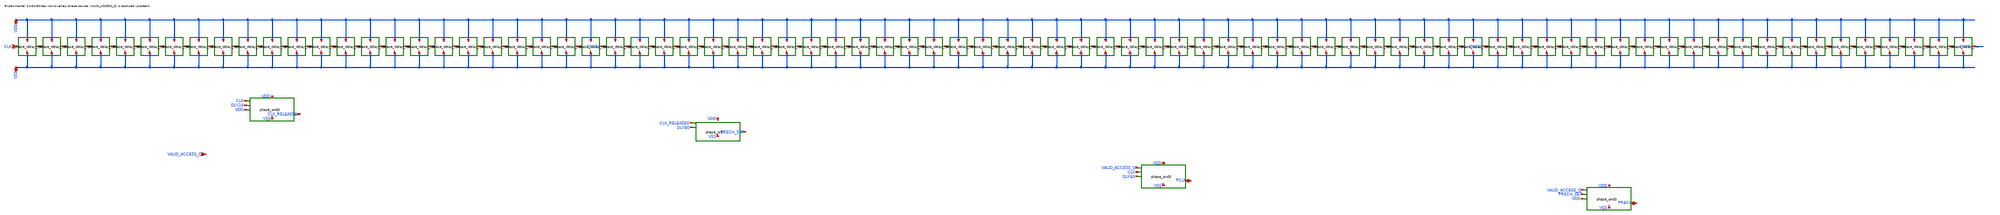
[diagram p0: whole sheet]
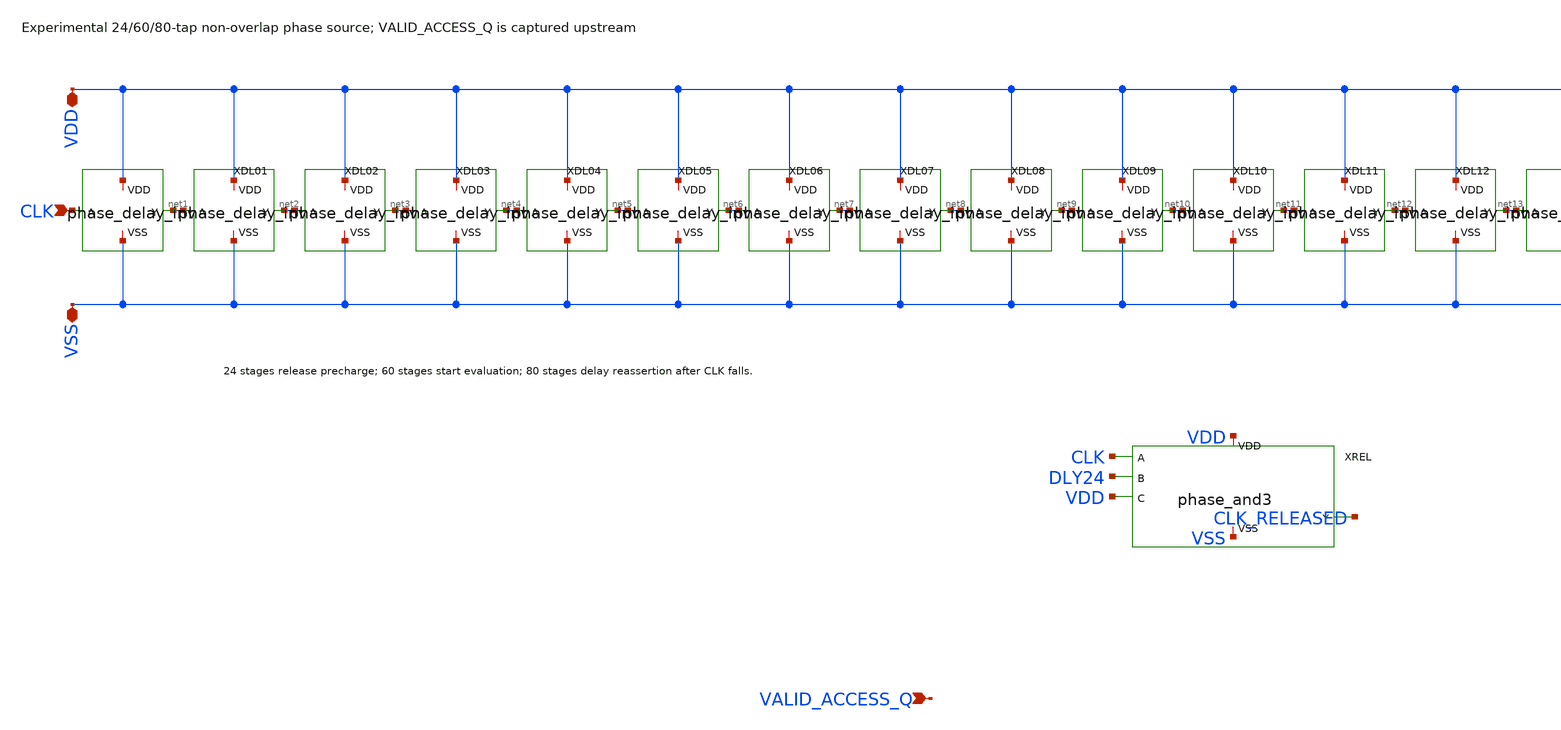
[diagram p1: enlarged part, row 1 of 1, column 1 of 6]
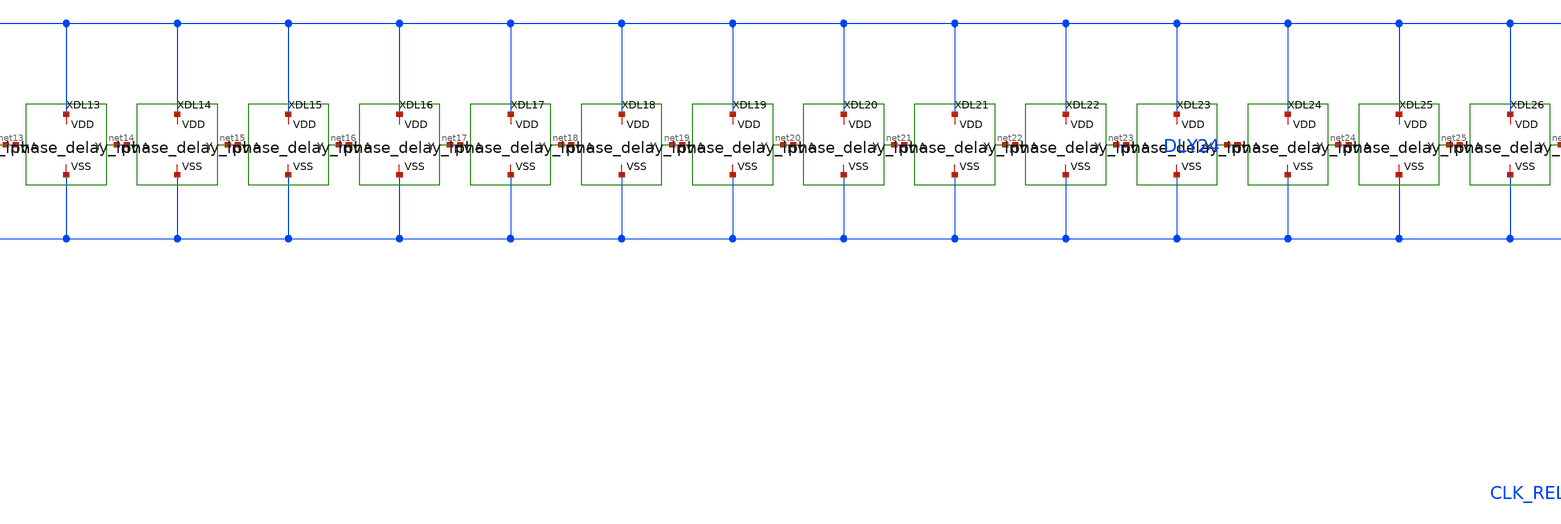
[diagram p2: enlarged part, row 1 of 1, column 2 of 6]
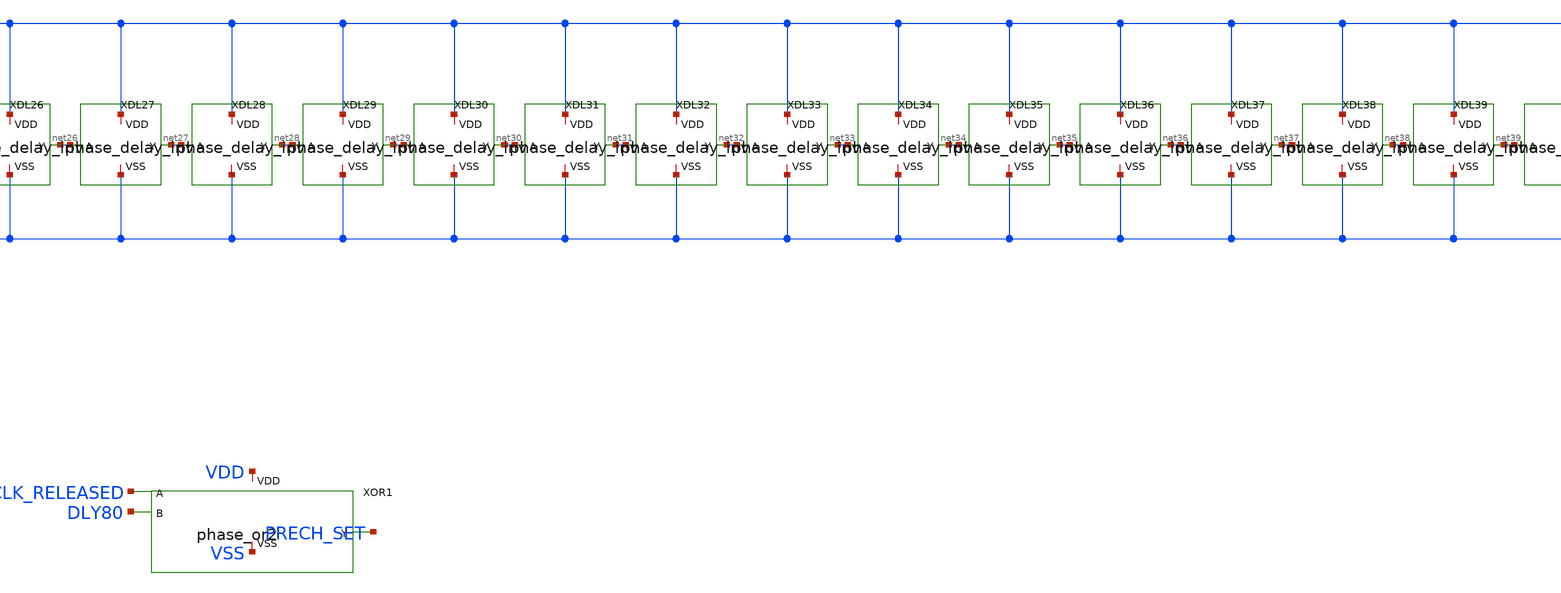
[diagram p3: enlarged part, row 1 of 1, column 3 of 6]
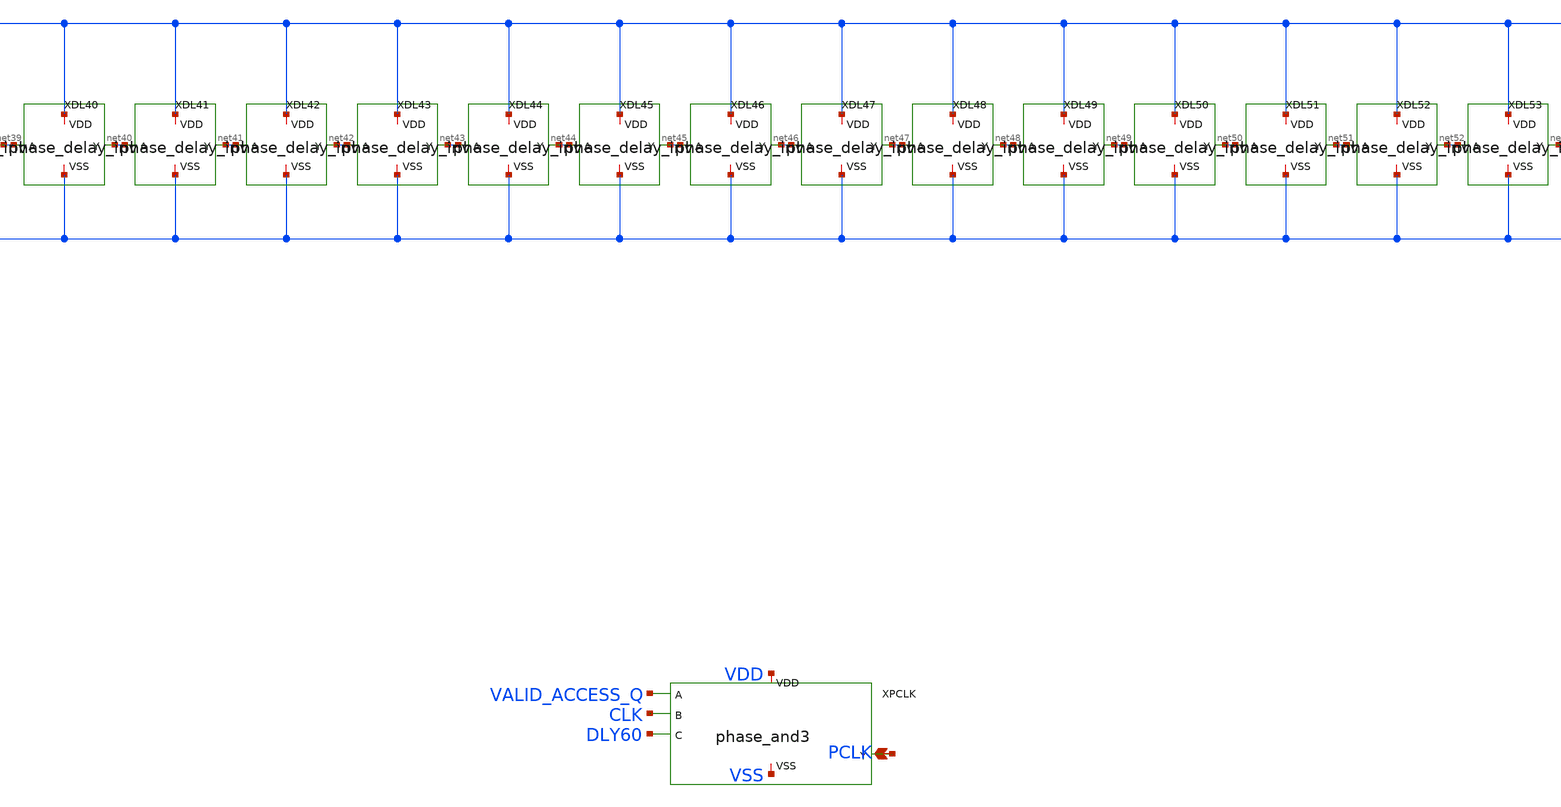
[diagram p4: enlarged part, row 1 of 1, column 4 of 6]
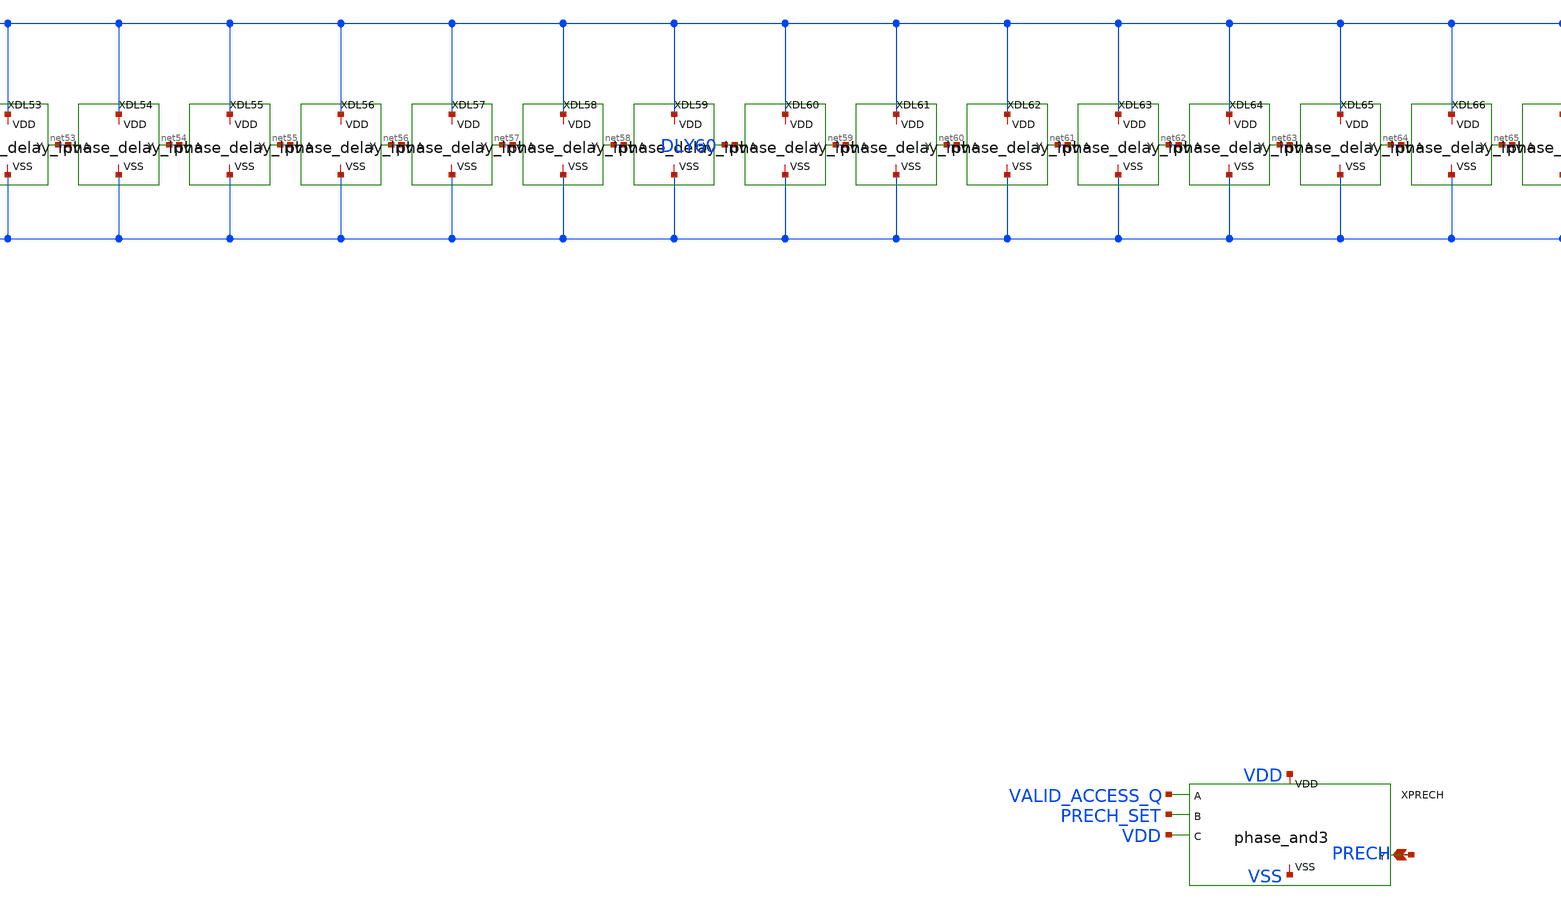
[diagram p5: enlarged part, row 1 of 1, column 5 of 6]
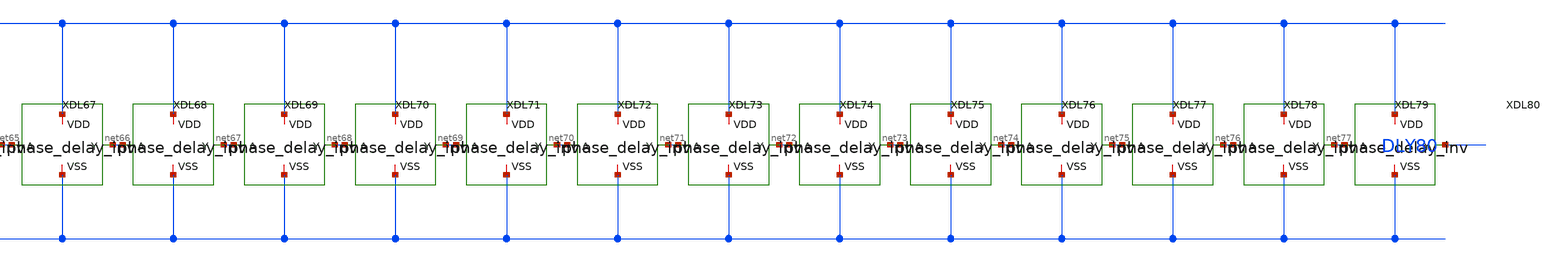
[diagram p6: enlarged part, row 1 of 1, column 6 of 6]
** sch_path: cells/control/pclk_phase_source.sch
**.subckt pclk_phase_source CLK VDD VSS VALID_ACCESS_Q PCLK PRECH
*.ipin CLK
*.iopin VDD
*.iopin VSS
*.ipin VALID_ACCESS_Q
*.opin PCLK
*.opin PRECH
XDL01 VDD CLK net1 VSS phase_delay_inv
XDL02 VDD net1 net2 VSS phase_delay_inv
XDL03 VDD net2 net3 VSS phase_delay_inv
XDL04 VDD net3 net4 VSS phase_delay_inv
XDL05 VDD net4 net5 VSS phase_delay_inv
XDL06 VDD net5 net6 VSS phase_delay_inv
XDL07 VDD net6 net7 VSS phase_delay_inv
XDL08 VDD net7 net8 VSS phase_delay_inv
XDL09 VDD net8 net9 VSS phase_delay_inv
XDL10 VDD net9 net10 VSS phase_delay_inv
XDL11 VDD net10 net11 VSS phase_delay_inv
XDL12 VDD net11 net12 VSS phase_delay_inv
XDL13 VDD net12 net13 VSS phase_delay_inv
XDL14 VDD net13 net14 VSS phase_delay_inv
XDL15 VDD net14 net15 VSS phase_delay_inv
XDL16 VDD net15 net16 VSS phase_delay_inv
XDL17 VDD net16 net17 VSS phase_delay_inv
XDL18 VDD net17 net18 VSS phase_delay_inv
XDL19 VDD net18 net19 VSS phase_delay_inv
XDL20 VDD net19 net20 VSS phase_delay_inv
XDL21 VDD net20 net21 VSS phase_delay_inv
XDL22 VDD net21 net22 VSS phase_delay_inv
XDL23 VDD net22 net23 VSS phase_delay_inv
XDL24 VDD net23 DLY24 VSS phase_delay_inv
XDL25 VDD DLY24 net24 VSS phase_delay_inv
XDL26 VDD net24 net25 VSS phase_delay_inv
XDL27 VDD net25 net26 VSS phase_delay_inv
XDL28 VDD net26 net27 VSS phase_delay_inv
XDL29 VDD net27 net28 VSS phase_delay_inv
XDL30 VDD net28 net29 VSS phase_delay_inv
XDL31 VDD net29 net30 VSS phase_delay_inv
XDL32 VDD net30 net31 VSS phase_delay_inv
XDL33 VDD net31 net32 VSS phase_delay_inv
XDL34 VDD net32 net33 VSS phase_delay_inv
XDL35 VDD net33 net34 VSS phase_delay_inv
XDL36 VDD net34 net35 VSS phase_delay_inv
XDL37 VDD net35 net36 VSS phase_delay_inv
XDL38 VDD net36 net37 VSS phase_delay_inv
XDL39 VDD net37 net38 VSS phase_delay_inv
XDL40 VDD net38 net39 VSS phase_delay_inv
XDL41 VDD net39 net40 VSS phase_delay_inv
XDL42 VDD net40 net41 VSS phase_delay_inv
XDL43 VDD net41 net42 VSS phase_delay_inv
XDL44 VDD net42 net43 VSS phase_delay_inv
XDL45 VDD net43 net44 VSS phase_delay_inv
XDL46 VDD net44 net45 VSS phase_delay_inv
XDL47 VDD net45 net46 VSS phase_delay_inv
XDL48 VDD net46 net47 VSS phase_delay_inv
XDL49 VDD net47 net48 VSS phase_delay_inv
XDL50 VDD net48 net49 VSS phase_delay_inv
XDL51 VDD net49 net50 VSS phase_delay_inv
XDL52 VDD net50 net51 VSS phase_delay_inv
XDL53 VDD net51 net52 VSS phase_delay_inv
XDL54 VDD net52 net53 VSS phase_delay_inv
XDL55 VDD net53 net54 VSS phase_delay_inv
XDL56 VDD net54 net55 VSS phase_delay_inv
XDL57 VDD net55 net56 VSS phase_delay_inv
XDL58 VDD net56 net57 VSS phase_delay_inv
XDL59 VDD net57 net58 VSS phase_delay_inv
XDL60 VDD net58 DLY60 VSS phase_delay_inv
XDL61 VDD DLY60 net59 VSS phase_delay_inv
XDL62 VDD net59 net60 VSS phase_delay_inv
XDL63 VDD net60 net61 VSS phase_delay_inv
XDL64 VDD net61 net62 VSS phase_delay_inv
XDL65 VDD net62 net63 VSS phase_delay_inv
XDL66 VDD net63 net64 VSS phase_delay_inv
XDL67 VDD net64 net65 VSS phase_delay_inv
XDL68 VDD net65 net66 VSS phase_delay_inv
XDL69 VDD net66 net67 VSS phase_delay_inv
XDL70 VDD net67 net68 VSS phase_delay_inv
XDL71 VDD net68 net69 VSS phase_delay_inv
XDL72 VDD net69 net70 VSS phase_delay_inv
XDL73 VDD net70 net71 VSS phase_delay_inv
XDL74 VDD net71 net72 VSS phase_delay_inv
XDL75 VDD net72 net73 VSS phase_delay_inv
XDL76 VDD net73 net74 VSS phase_delay_inv
XDL77 VDD net74 net75 VSS phase_delay_inv
XDL78 VDD net75 net76 VSS phase_delay_inv
XDL79 VDD net76 net77 VSS phase_delay_inv
XDL80 VDD net77 DLY80 VSS phase_delay_inv
XREL VDD CLK DLY24 VDD CLK_RELEASED VSS phase_and3
XOR1 VDD CLK_RELEASED DLY80 PRECH_SET VSS phase_or2
XPCLK VDD VALID_ACCESS_Q CLK DLY60 PCLK VSS phase_and3
XPRECH VDD VALID_ACCESS_Q PRECH_SET VDD PRECH VSS phase_and3
**.ends

* expanding   symbol:  phase_delay_inv.sym # of pins=4
** sym_path: cells/control/phase_delay_inv.sym
** sch_path: cells/control/phase_delay_inv.sch
.subckt phase_delay_inv VDD A Y VSS
*.ipin A
*.opin Y
*.iopin VDD
*.iopin VSS
XMP Y A VDD VDD sky130_fd_pr__pfet_01v8 L=0.15 W=1.26 nf=1 ad='int((nf+1)/2) * W/nf * 0.29' as='int((nf+2)/2) * W/nf * 0.29'
+ pd='2*int((nf+1)/2) * (W/nf + 0.29)' ps='2*int((nf+2)/2) * (W/nf + 0.29)' nrd='0.29 / W' nrs='0.29 / W'
+ sa=0 sb=0 sd=0 mult=1 m=1
XMN Y A VSS VSS sky130_fd_pr__nfet_01v8 L=0.15 W=0.42 nf=1 ad='int((1 + 1)/2) * 0.42 / 1 * 0.29' as='int((1 + 2)/2) * 0.42 / 1 * 0.29'
+ pd='2*int((1 + 1)/2) * (0.42 / 1 + 0.29)' ps='2*int((1 + 2)/2) * (0.42 / 1 + 0.29)' nrd='0.29 / 0.42 '
+ nrs='0.29 / 0.42 ' sa=0 sb=0 sd=0 mult=1 m=1
.ends


* expanding   symbol:  phase_and3.sym # of pins=6
** sym_path: cells/control/phase_and3.sym
** sch_path: cells/control/phase_and3.sch
.subckt phase_and3 VDD A B C Y VSS
*.iopin VDD
*.ipin A
*.ipin B
*.ipin C
*.opin Y
*.iopin VSS
XMPA NAND3 A VDD VDD sky130_fd_pr__pfet_01v8 L=0.15 W=0.84 nf=1 ad='int((nf+1)/2) * W/nf * 0.29' as='int((nf+2)/2) * W/nf * 0.29'
+ pd='2*int((nf+1)/2) * (W/nf + 0.29)' ps='2*int((nf+2)/2) * (W/nf + 0.29)' nrd='0.29 / W' nrs='0.29 / W'
+ sa=0 sb=0 sd=0 mult=1 m=1
XMPB NAND3 B VDD VDD sky130_fd_pr__pfet_01v8 L=0.15 W=0.84 nf=1 ad='int((nf+1)/2) * W/nf * 0.29' as='int((nf+2)/2) * W/nf * 0.29'
+ pd='2*int((nf+1)/2) * (W/nf + 0.29)' ps='2*int((nf+2)/2) * (W/nf + 0.29)' nrd='0.29 / W' nrs='0.29 / W'
+ sa=0 sb=0 sd=0 mult=1 m=1
XMPC NAND3 C VDD VDD sky130_fd_pr__pfet_01v8 L=0.15 W=0.84 nf=1 ad='int((nf+1)/2) * W/nf * 0.29' as='int((nf+2)/2) * W/nf * 0.29'
+ pd='2*int((nf+1)/2) * (W/nf + 0.29)' ps='2*int((nf+2)/2) * (W/nf + 0.29)' nrd='0.29 / W' nrs='0.29 / W'
+ sa=0 sb=0 sd=0 mult=1 m=1
XMNA NAND3 A net1 VSS sky130_fd_pr__nfet_01v8 L=0.15 W=0.42 nf=1 ad='int((1 + 1)/2) * 0.42 / 1 * 0.29'
+ as='int((1 + 2)/2) * 0.42 / 1 * 0.29' pd='2*int((1 + 1)/2) * (0.42 / 1 + 0.29)' ps='2*int((1 + 2)/2) * (0.42 / 1 + 0.29)'
+ nrd='0.29 / 0.42 ' nrs='0.29 / 0.42 ' sa=0 sb=0 sd=0 mult=1 m=1
XMNB net1 B net2 VSS sky130_fd_pr__nfet_01v8 L=0.15 W=0.42 nf=1 ad='int((1 + 1)/2) * 0.42 / 1 * 0.29'
+ as='int((1 + 2)/2) * 0.42 / 1 * 0.29' pd='2*int((1 + 1)/2) * (0.42 / 1 + 0.29)' ps='2*int((1 + 2)/2) * (0.42 / 1 + 0.29)'
+ nrd='0.29 / 0.42 ' nrs='0.29 / 0.42 ' sa=0 sb=0 sd=0 mult=1 m=1
XMNC net2 C VSS VSS sky130_fd_pr__nfet_01v8 L=0.15 W=0.42 nf=1 ad='int((1 + 1)/2) * 0.42 / 1 * 0.29'
+ as='int((1 + 2)/2) * 0.42 / 1 * 0.29' pd='2*int((1 + 1)/2) * (0.42 / 1 + 0.29)' ps='2*int((1 + 2)/2) * (0.42 / 1 + 0.29)'
+ nrd='0.29 / 0.42 ' nrs='0.29 / 0.42 ' sa=0 sb=0 sd=0 mult=1 m=1
XMPINV Y NAND3 VDD VDD sky130_fd_pr__pfet_01v8 L=0.15 W=3.0 nf=1 ad='int((nf+1)/2) * W/nf * 0.29' as='int((nf+2)/2) * W/nf * 0.29'
+ pd='2*int((nf+1)/2) * (W/nf + 0.29)' ps='2*int((nf+2)/2) * (W/nf + 0.29)' nrd='0.29 / W' nrs='0.29 / W'
+ sa=0 sb=0 sd=0 mult=1 m=1
XMNINV Y NAND3 VSS VSS sky130_fd_pr__nfet_01v8 L=0.15 W=1.5 nf=1 ad='int((1 + 1)/2) * 1.5 / 1 * 0.29'
+ as='int((1 + 2)/2) * 1.5 / 1 * 0.29' pd='2*int((1 + 1)/2) * (1.5 / 1 + 0.29)' ps='2*int((1 + 2)/2) * (1.5 / 1 + 0.29)'
+ nrd='0.29 / 1.5 ' nrs='0.29 / 1.5 ' sa=0 sb=0 sd=0 mult=1 m=1
.ends


* expanding   symbol:  phase_or2.sym # of pins=5
** sym_path: cells/control/phase_or2.sym
** sch_path: cells/control/phase_or2.sch
.subckt phase_or2 VDD A B Y VSS
*.iopin VDD
*.ipin A
*.ipin B
*.opin Y
*.iopin VSS
XMPA net1 A VDD VDD sky130_fd_pr__pfet_01v8 L=0.15 W=1.68 nf=1 ad='int((nf+1)/2) * W/nf * 0.29' as='int((nf+2)/2) * W/nf * 0.29'
+ pd='2*int((nf+1)/2) * (W/nf + 0.29)' ps='2*int((nf+2)/2) * (W/nf + 0.29)' nrd='0.29 / W' nrs='0.29 / W'
+ sa=0 sb=0 sd=0 mult=1 m=1
XMPB NOR2 B net1 VDD sky130_fd_pr__pfet_01v8 L=0.15 W=1.68 nf=1 ad='int((nf+1)/2) * W/nf * 0.29' as='int((nf+2)/2) * W/nf * 0.29'
+ pd='2*int((nf+1)/2) * (W/nf + 0.29)' ps='2*int((nf+2)/2) * (W/nf + 0.29)' nrd='0.29 / W' nrs='0.29 / W'
+ sa=0 sb=0 sd=0 mult=1 m=1
XMNA NOR2 A VSS VSS sky130_fd_pr__nfet_01v8 L=0.15 W=0.42 nf=1 ad='int((1 + 1)/2) * 0.42 / 1 * 0.29'
+ as='int((1 + 2)/2) * 0.42 / 1 * 0.29' pd='2*int((1 + 1)/2) * (0.42 / 1 + 0.29)' ps='2*int((1 + 2)/2) * (0.42 / 1 + 0.29)'
+ nrd='0.29 / 0.42 ' nrs='0.29 / 0.42 ' sa=0 sb=0 sd=0 mult=1 m=1
XMNB NOR2 B VSS VSS sky130_fd_pr__nfet_01v8 L=0.15 W=0.42 nf=1 ad='int((1 + 1)/2) * 0.42 / 1 * 0.29'
+ as='int((1 + 2)/2) * 0.42 / 1 * 0.29' pd='2*int((1 + 1)/2) * (0.42 / 1 + 0.29)' ps='2*int((1 + 2)/2) * (0.42 / 1 + 0.29)'
+ nrd='0.29 / 0.42 ' nrs='0.29 / 0.42 ' sa=0 sb=0 sd=0 mult=1 m=1
XMPINV Y NOR2 VDD VDD sky130_fd_pr__pfet_01v8 L=0.15 W=3.0 nf=1 ad='int((nf+1)/2) * W/nf * 0.29' as='int((nf+2)/2) * W/nf * 0.29'
+ pd='2*int((nf+1)/2) * (W/nf + 0.29)' ps='2*int((nf+2)/2) * (W/nf + 0.29)' nrd='0.29 / W' nrs='0.29 / W'
+ sa=0 sb=0 sd=0 mult=1 m=1
XMNINV Y NOR2 VSS VSS sky130_fd_pr__nfet_01v8 L=0.15 W=1.5 nf=1 ad='int((1 + 1)/2) * 1.5 / 1 * 0.29'
+ as='int((1 + 2)/2) * 1.5 / 1 * 0.29' pd='2*int((1 + 1)/2) * (1.5 / 1 + 0.29)' ps='2*int((1 + 2)/2) * (1.5 / 1 + 0.29)'
+ nrd='0.29 / 1.5 ' nrs='0.29 / 1.5 ' sa=0 sb=0 sd=0 mult=1 m=1
.ends

.end
